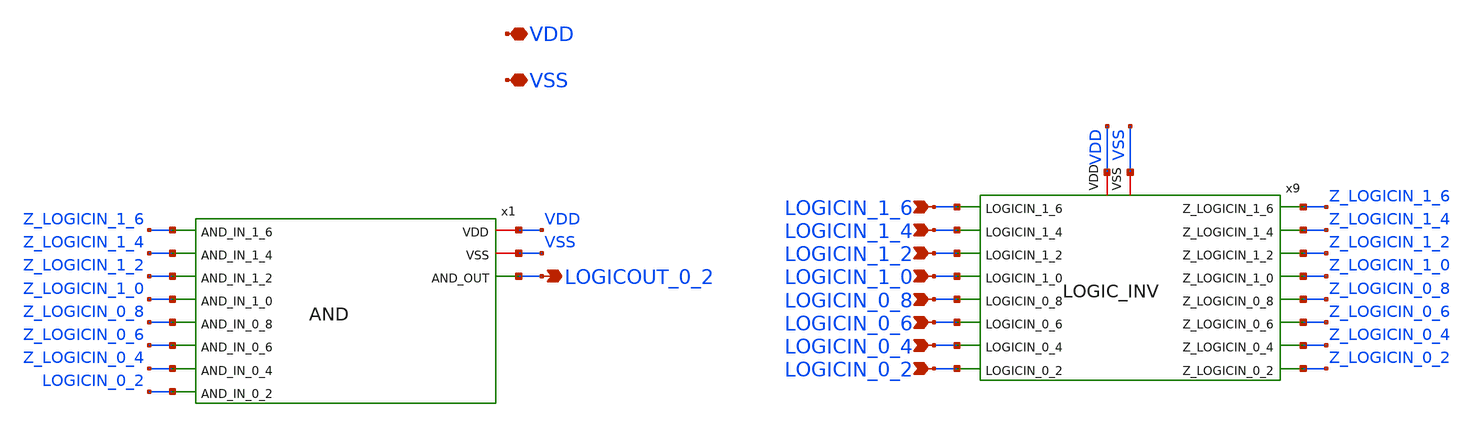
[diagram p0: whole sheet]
** sch_path: xschem/logic_fix1.sch
**.subckt logic_fix1 LOGICOUT_0_2 LOGICIN_1_0 LOGICIN_1_2 LOGICIN_1_4 LOGICIN_1_6 LOGICIN_0_2
*+ LOGICIN_0_4 LOGICIN_0_6 LOGICIN_0_8 VDD VSS
*.opin LOGICOUT_0_2
*.ipin LOGICIN_1_0
*.ipin LOGICIN_1_2
*.ipin LOGICIN_1_4
*.ipin LOGICIN_1_6
*.ipin LOGICIN_0_2
*.ipin LOGICIN_0_4
*.ipin LOGICIN_0_6
*.ipin LOGICIN_0_8
*.iopin VDD
*.iopin VSS
x1 VDD VSS Z_LOGICIN_1_6 Z_LOGICIN_1_4 Z_LOGICIN_1_2 Z_LOGICIN_1_0 LOGICOUT_0_2 Z_LOGICIN_0_8
+ Z_LOGICIN_0_6 Z_LOGICIN_0_4 LOGICIN_0_2 AND
x9 LOGICIN_1_6 Z_LOGICIN_1_6 Z_LOGICIN_1_4 LOGICIN_1_4 LOGICIN_1_2 Z_LOGICIN_1_2 LOGICIN_1_0
+ Z_LOGICIN_1_0 Z_LOGICIN_0_8 LOGICIN_0_8 Z_LOGICIN_0_6 LOGICIN_0_6 LOGICIN_0_4 Z_LOGICIN_0_4 LOGICIN_0_2
+ Z_LOGICIN_0_2 VDD VSS LOGIC_INV
**.ends
.end
